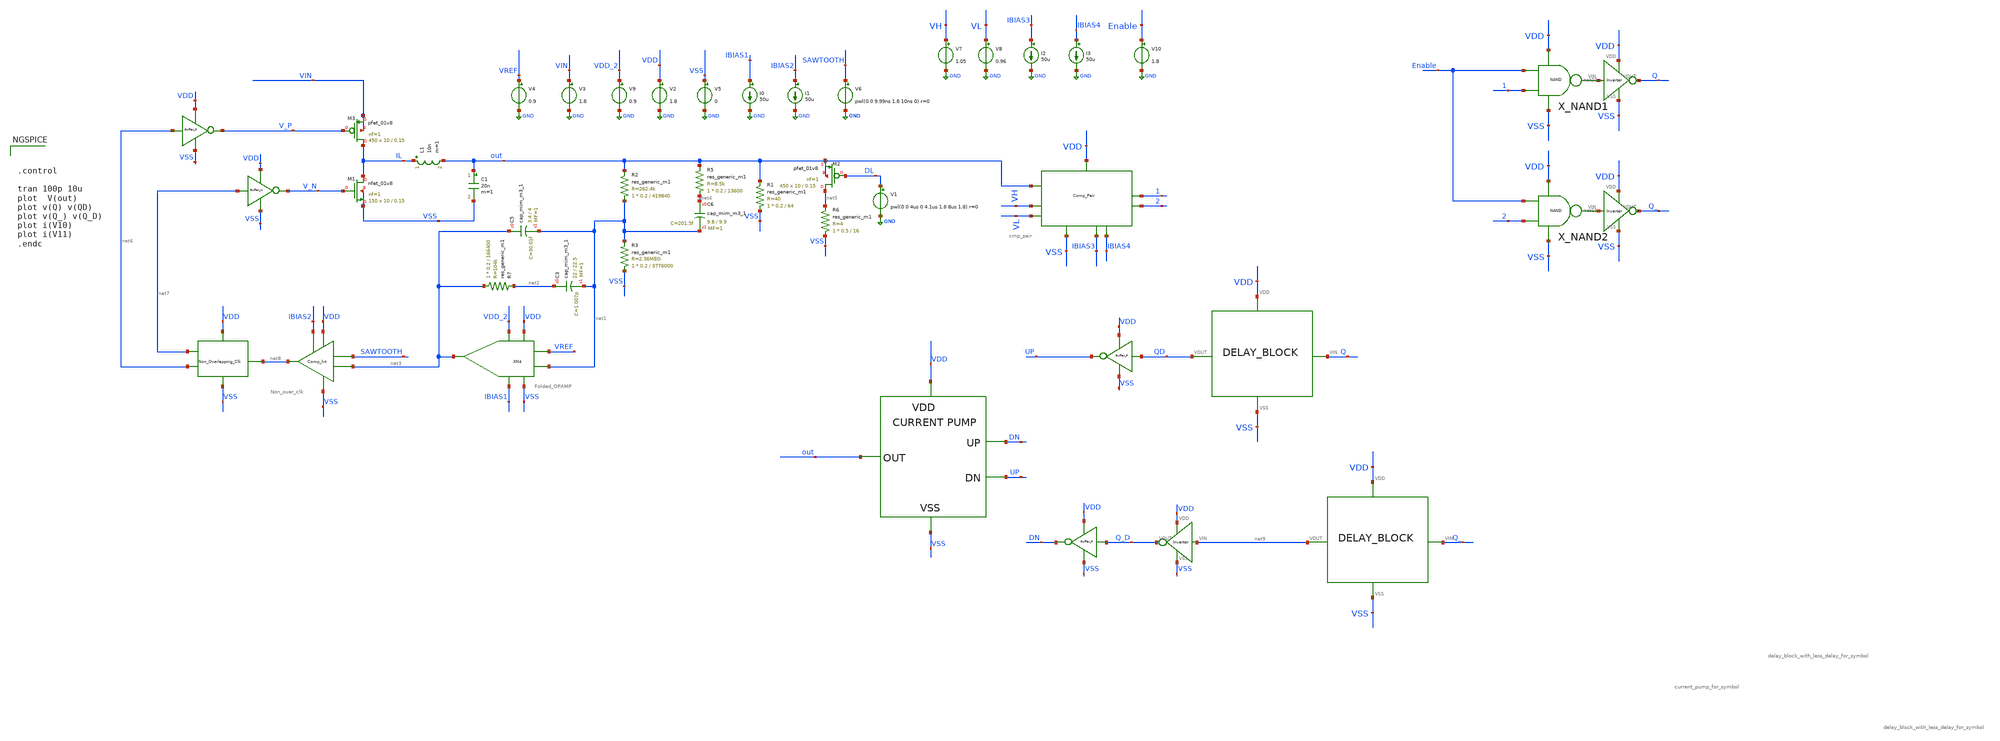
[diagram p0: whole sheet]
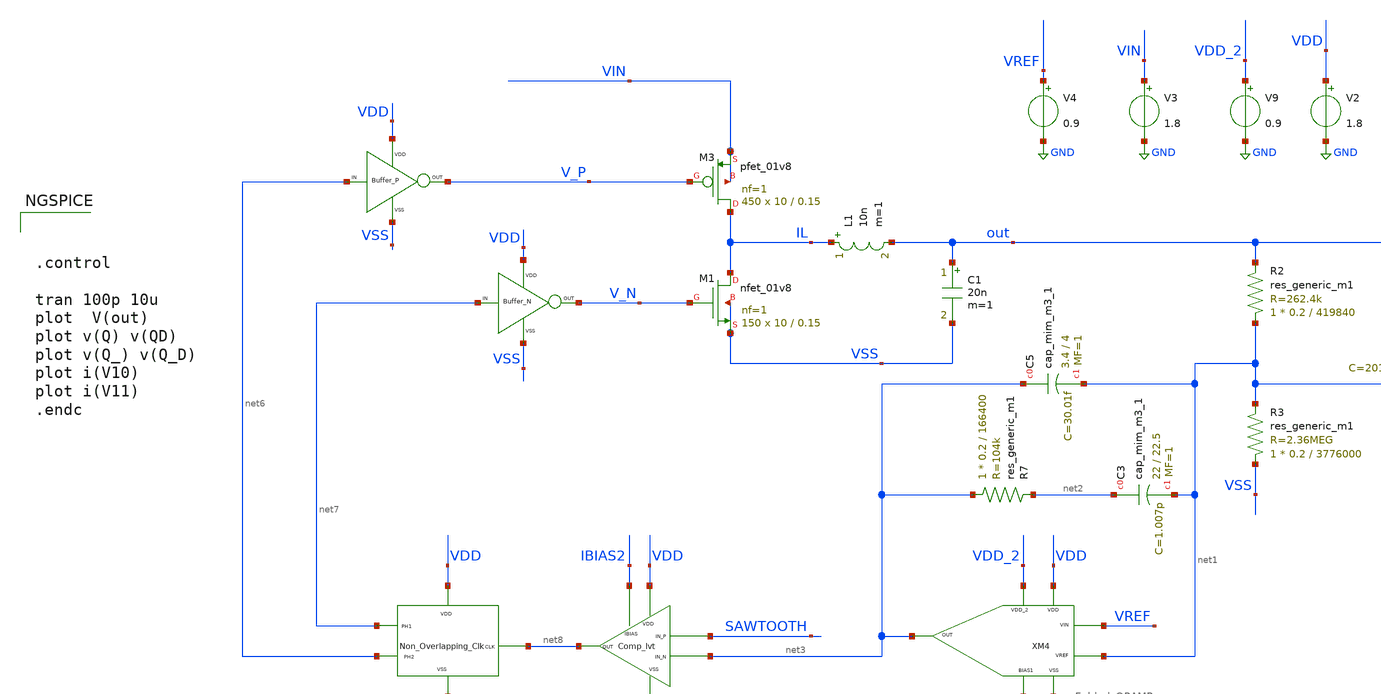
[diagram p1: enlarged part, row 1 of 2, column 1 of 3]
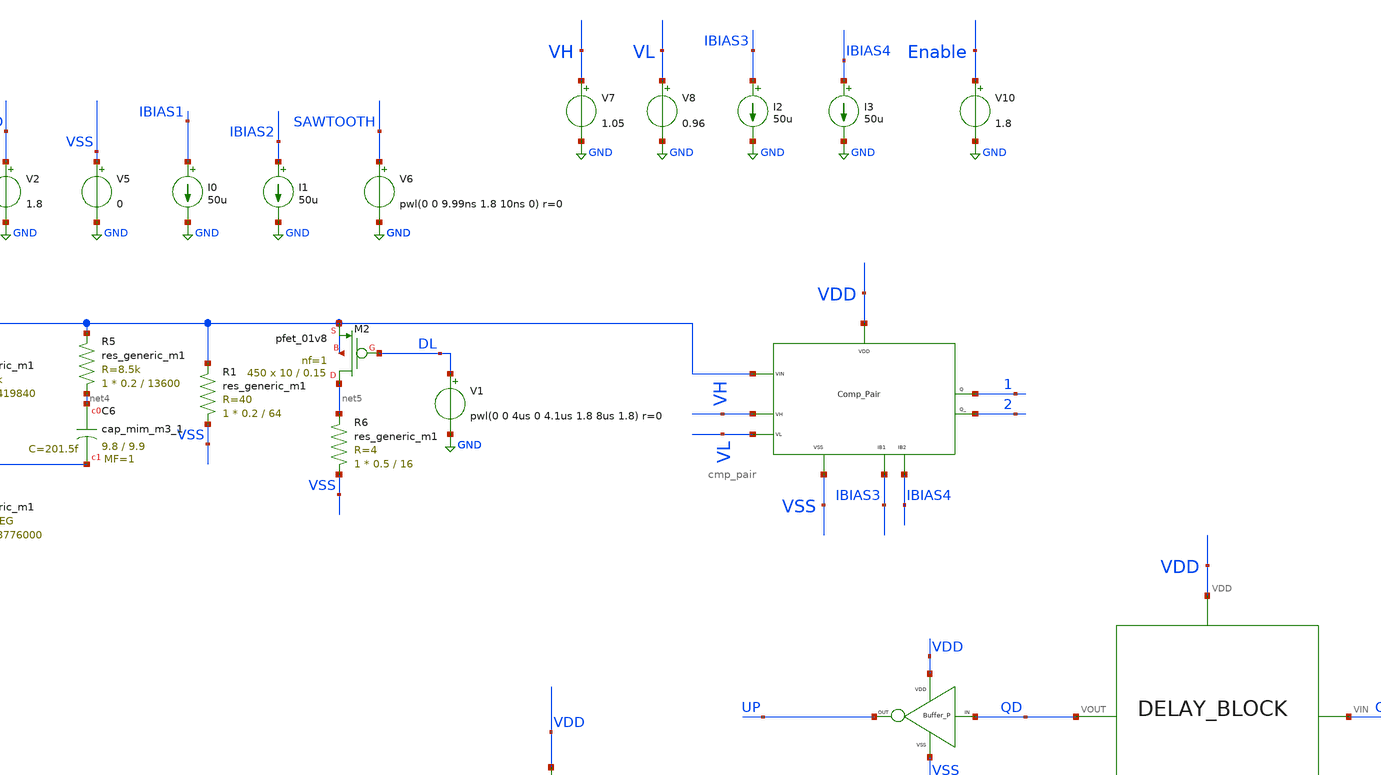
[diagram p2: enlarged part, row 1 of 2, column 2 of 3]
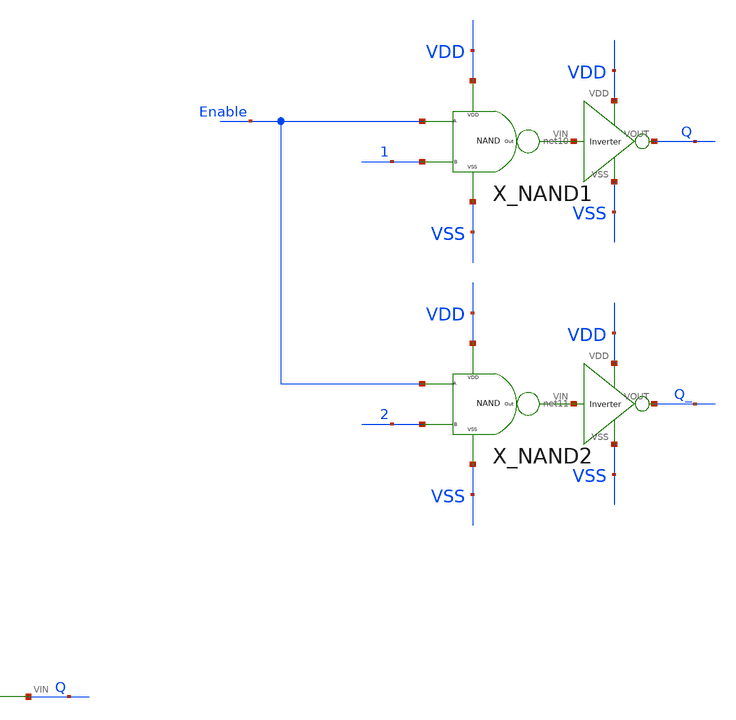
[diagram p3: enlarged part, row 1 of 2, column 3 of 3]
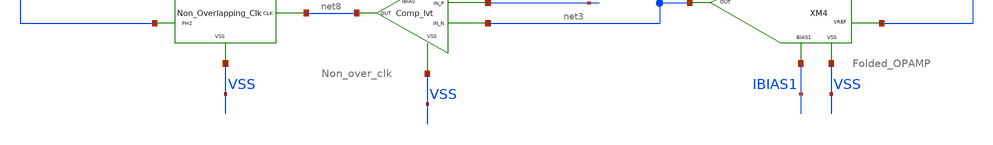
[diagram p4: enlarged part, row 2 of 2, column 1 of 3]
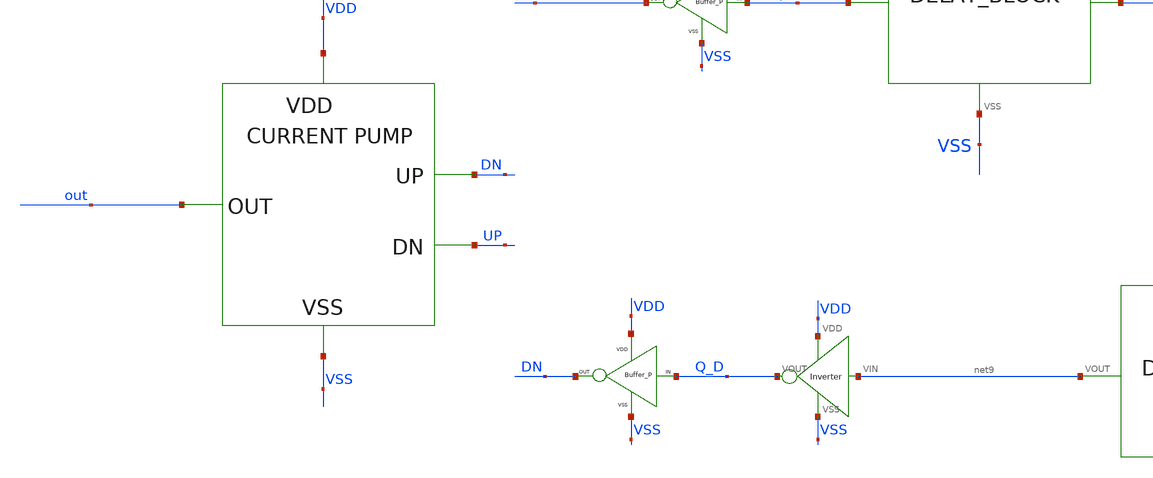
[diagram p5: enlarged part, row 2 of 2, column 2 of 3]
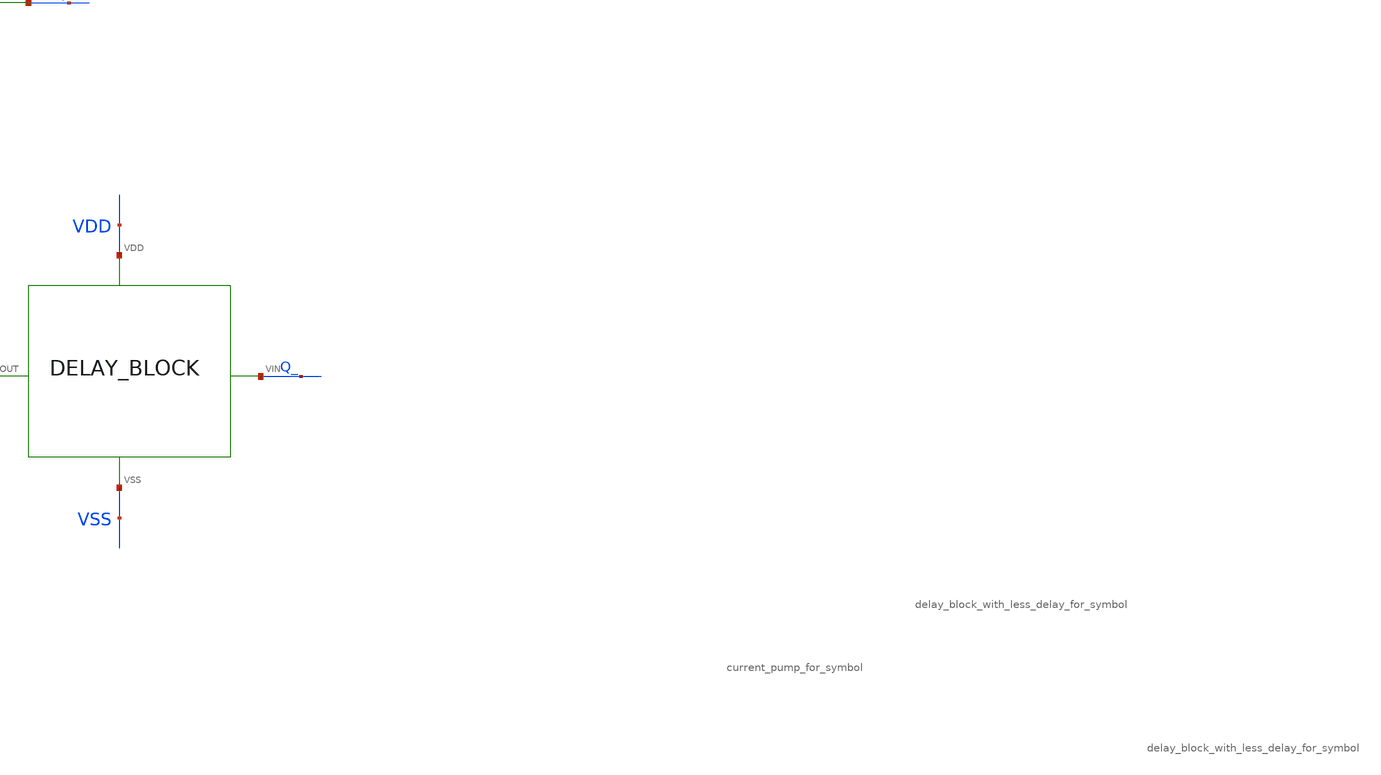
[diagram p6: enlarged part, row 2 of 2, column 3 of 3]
** sch_path: xschem/DC_DC_Converter_xschem/OTHERS/DC_DC_Converter_4/TOP_LEVEL/closed_loop_v10.sch
**.subckt closed_loop_v10
XM3 IL V_P VIN VIN sky130_fd_pr__pfet_01v8 L=0.15 W=10 nf=1 ad='int((nf+1)/2) * W/nf * 0.29' as='int((nf+2)/2) * W/nf * 0.29'
+ pd='2*int((nf+1)/2) * (W/nf + 0.29)' ps='2*int((nf+2)/2) * (W/nf + 0.29)' nrd='0.29 / W' nrs='0.29 / W'
+ sa=0 sb=0 sd=0 mult=450 m=450
L1 IL out 10n m=1
C1 out VSS 20n m=1
V3 VIN GND 1.8
I0 IBIAS1 GND 50u
V9 VDD_2 GND 0.9
V2 VDD GND 1.8
V5 VSS GND 0
V4 VREF GND 0.9
I1 IBIAS2 GND 50u
V6 SAWTOOTH GND pwl(0 0 9.99ns 1.8 10ns 0) r=0
XM1 IL V_N VSS VSS sky130_fd_pr__nfet_01v8 L=0.15 W=10 nf=1 ad='int((nf+1)/2) * W/nf * 0.29' as='int((nf+2)/2) * W/nf * 0.29'
+ pd='2*int((nf+1)/2) * (W/nf + 0.29)' ps='2*int((nf+2)/2) * (W/nf + 0.29)' nrd='0.29 / W' nrs='0.29 / W'
+ sa=0 sb=0 sd=0 mult=150 m=150
XM2 net5 DL out out sky130_fd_pr__pfet_01v8 L=0.15 W=10 nf=1 ad='int((nf+1)/2) * W/nf * 0.29' as='int((nf+2)/2) * W/nf * 0.29'
+ pd='2*int((nf+1)/2) * (W/nf + 0.29)' ps='2*int((nf+2)/2) * (W/nf + 0.29)' nrd='0.29 / W' nrs='0.29 / W'
+ sa=0 sb=0 sd=0 mult=450 m=450
V1 DL GND pwl(0 0 4us 0 4.1us 1.8 8us 1.8) r=0
X1 net6 V_P VDD VSS BUFFER_P
X2 net7 V_N VDD VSS BUFFER_N
XM3 net8 VDD VSS net7 net6 Non_over_clk
XM4 VDD VSS VDD_2 IBIAS1 net3 VREF net1 Folded_OPAMP
XM2 IBIAS2 VDD SAWTOOTH net3 VSS net8 Comp_lvt
V7 VH GND 1.05
V8 VL GND 0.96
I2 IBIAS3 GND 50u
I3 IBIAS4 GND 50u
XM1 VDD VSS out VH VL IBIAS3 IBIAS4 1 2 cmp_pair
X3 Q QD VDD VSS delay_block_with_less_delay_for_symbol
X4 Q_ net9 VDD VSS delay_block_with_less_delay_for_symbol
X5 QD UP VDD VSS BUFFER_P
X6 Q_D DN VDD VSS BUFFER_P
X7 DN out VDD VSS UP current_pump_for_symbol
X8 VSS VDD net9 Q_D Inverter
X_NAND1 VDD VSS Enable 1 net10 NAND
X_NAND2 VDD VSS Enable 2 net11 NAND
X9 VSS VDD net10 Q Inverter
X10 VSS VDD net11 Q_ Inverter
XC5 net3 net1 sky130_fd_pr__cap_mim_m3_1 W=3.4 L=4 MF=1 m=1
XC3 net2 net1 sky130_fd_pr__cap_mim_m3_1 W=22 L=22.5 MF=1 m=1
R7 net3 net2 sky130_fd_pr__res_generic_m1 W=0.2 L=166400 m=1
R6 VSS net5 sky130_fd_pr__res_generic_m1 W=0.5 L=16 m=1
R1 VSS out sky130_fd_pr__res_generic_m1 W=0.2 L=64 m=1
R5 net4 out sky130_fd_pr__res_generic_m1 W=0.2 L=13600 m=1
R2 net1 out sky130_fd_pr__res_generic_m1 W=0.2 L=419840 m=1
R3 VSS net1 sky130_fd_pr__res_generic_m1 W=0.2 L=3776000 m=1
V10 Enable GND 1.8
XC6 net4 net1 sky130_fd_pr__cap_mim_m3_1 W=9.8 L=9.9 MF=1 m=1
**** begin user architecture code

** opencircuitdesign pdks install
.lib $::SKYWATER_MODELS/sky130.lib.spice tt





.control

tran 100p 10u
plot  V(out)
plot v(Q) v(QD)
plot v(Q_) v(Q_D)
plot i(V10)
plot i(V11)
.endc


**** end user architecture code
**.ends
.GLOBAL GND
.end
